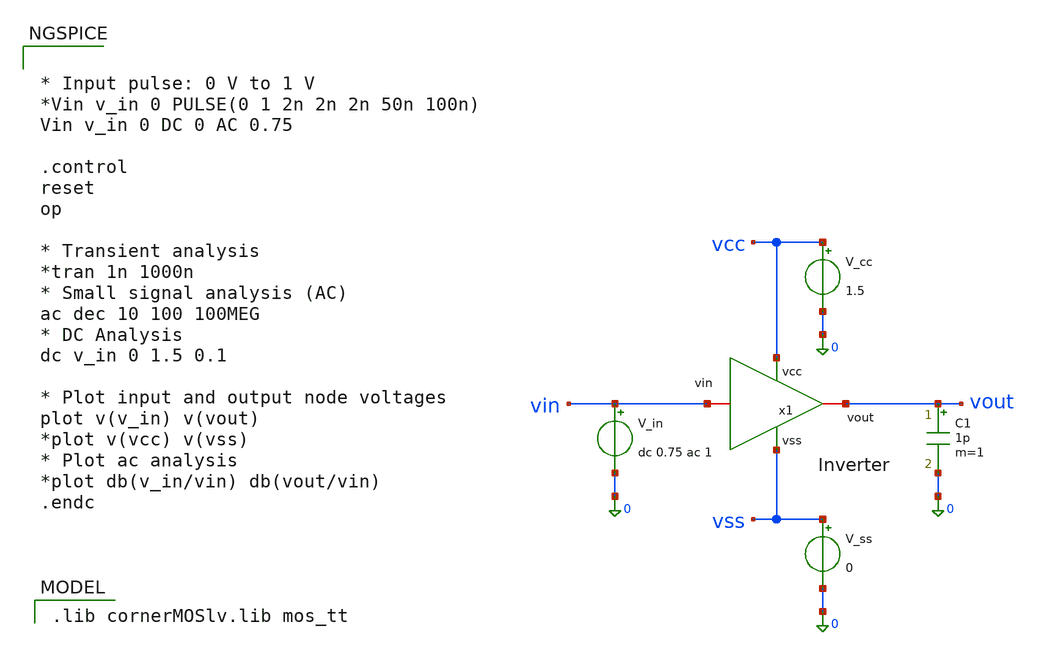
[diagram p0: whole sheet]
** sch_path: 001_Inverter/Inverter_tb.sch
**.subckt Inverter_tb
x1 vcc vin vout vss Inverter
V_cc vcc 0 1.5
V_ss vss 0 0
V_in vin 0 dc 0.75 ac 1
C1 vout 0 1p m=1
**** begin user architecture code


* Input pulse: 0 V to 1 V
*Vin v_in 0 PULSE(0 1 2n 2n 2n 50n 100n)
Vin v_in 0 DC 0 AC 0.75

.control
reset
op

* Transient analysis
*tran 1n 1000n
* Small signal analysis (AC)
ac dec 10 100 100MEG
* DC Analysis
dc v_in 0 1.5 0.1

* Plot input and output node voltages
plot v(v_in) v(vout)
*plot v(vcc) v(vss)
* Plot ac analysis
*plot db(v_in/vin) db(vout/vin)
.endc


 .lib cornerMOSlv.lib mos_tt

**** end user architecture code
**.ends

* expanding   symbol:  DRMS/001_Inverter/Inverter.sym # of pins=4
** sym_path: 001_Inverter/Inverter.sym
** sch_path: 001_Inverter/Inverter.sch
.subckt Inverter vcc vin vout vss
*.iopin vin
*.iopin vout
*.ipin vcc
*.ipin vss
XM1 vout vin vss vss sg13_lv_nmos w=0.15u l=0.13u ng=1 m=1 mm_ok=1
XM2 vout vin vcc vcc sg13_lv_pmos w=0.15u l=0.13u ng=1 m=1 mm_ok=1
.ends

.end
